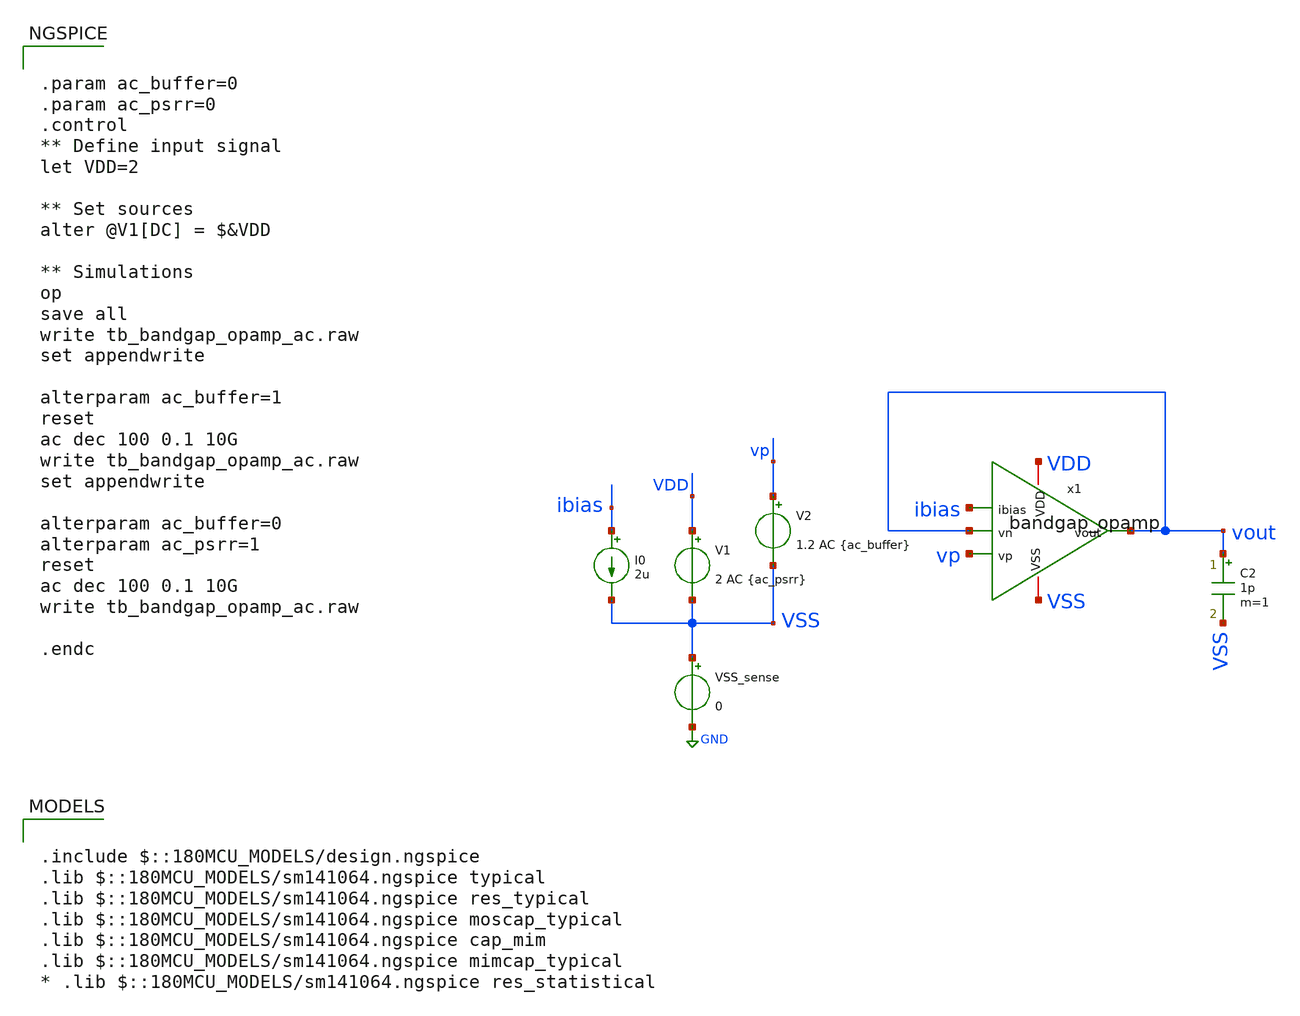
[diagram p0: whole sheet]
** sch_path: designs/libs/tb_bandgap/tb_bandgap_opamp_ac/tb_bandgap_opamp_ac.sch
**.subckt tb_bandgap_opamp_ac
V1 VDD VSS 2 AC {ac_psrr}
V2 vp VSS 1.2 AC {ac_buffer}
VSS_sense VSS GND 0
C2 vout VSS 1p m=1
I0 ibias VSS 2u
x1 VDD ibias vout vp vout VSS bandgap_opamp
**** begin user architecture code

.include $::180MCU_MODELS/design.ngspice
.lib $::180MCU_MODELS/sm141064.ngspice typical
.lib $::180MCU_MODELS/sm141064.ngspice res_typical
.lib $::180MCU_MODELS/sm141064.ngspice moscap_typical
.lib $::180MCU_MODELS/sm141064.ngspice cap_mim
.lib $::180MCU_MODELS/sm141064.ngspice mimcap_typical
* .lib $::180MCU_MODELS/sm141064.ngspice res_statistical



.param ac_buffer=0
.param ac_psrr=0
.control
** Define input signal
let VDD=2

** Set sources
alter @V1[DC] = $&VDD

** Simulations
op
save all
write tb_bandgap_opamp_ac.raw
set appendwrite

alterparam ac_buffer=1
reset
ac dec 100 0.1 10G
write tb_bandgap_opamp_ac.raw
set appendwrite

alterparam ac_buffer=0
alterparam ac_psrr=1
reset
ac dec 100 0.1 10G
write tb_bandgap_opamp_ac.raw

.endc


**** end user architecture code
**.ends
.GLOBAL GND
.end
